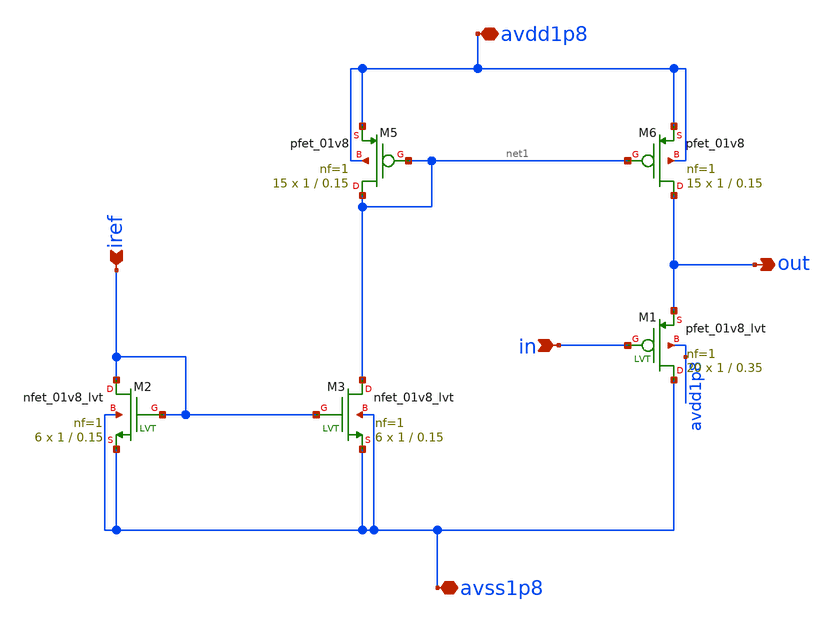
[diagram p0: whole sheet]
** sch_path: xschem/source_follower_buff_pmos.sch
**.subckt source_follower_buff_pmos avdd1p8 avss1p8 out in iref
*.iopin avdd1p8
*.iopin avss1p8
*.opin out
*.ipin in
*.ipin iref
XM5 net1 net1 avdd1p8 avdd1p8 sky130_fd_pr__pfet_01v8 L=0.15 W=1 nf=1 ad='int((nf+1)/2) * W/nf * 0.29'
+ as='int((nf+2)/2) * W/nf * 0.29' pd='2*int((nf+1)/2) * (W/nf + 0.29)' ps='2*int((nf+2)/2) * (W/nf + 0.29)'
+ nrd='0.29 / W' nrs='0.29 / W' sa=0 sb=0 sd=0 mult=15 m=15
XM6 out net1 avdd1p8 avdd1p8 sky130_fd_pr__pfet_01v8 L=0.15 W=1 nf=1 ad='int((nf+1)/2) * W/nf * 0.29'
+ as='int((nf+2)/2) * W/nf * 0.29' pd='2*int((nf+1)/2) * (W/nf + 0.29)' ps='2*int((nf+2)/2) * (W/nf + 0.29)'
+ nrd='0.29 / W' nrs='0.29 / W' sa=0 sb=0 sd=0 mult=15 m=15
XM1 avss1p8 in out avdd1p8 sky130_fd_pr__pfet_01v8_lvt L=0.35 W=1 nf=1 ad='int((nf+1)/2) * W/nf * 0.29'
+ as='int((nf+2)/2) * W/nf * 0.29' pd='2*int((nf+1)/2) * (W/nf + 0.29)' ps='2*int((nf+2)/2) * (W/nf + 0.29)'
+ nrd='0.29 / W' nrs='0.29 / W' sa=0 sb=0 sd=0 mult=20 m=20
XM2 iref iref avss1p8 avss1p8 sky130_fd_pr__nfet_01v8_lvt L=0.15 W=1 nf=1 ad='int((nf+1)/2) * W/nf * 0.29'
+ as='int((nf+2)/2) * W/nf * 0.29' pd='2*int((nf+1)/2) * (W/nf + 0.29)' ps='2*int((nf+2)/2) * (W/nf + 0.29)'
+ nrd='0.29 / W' nrs='0.29 / W' sa=0 sb=0 sd=0 mult=6 m=6
XM3 net1 iref avss1p8 avss1p8 sky130_fd_pr__nfet_01v8_lvt L=0.15 W=1 nf=1 ad='int((nf+1)/2) * W/nf * 0.29'
+ as='int((nf+2)/2) * W/nf * 0.29' pd='2*int((nf+1)/2) * (W/nf + 0.29)' ps='2*int((nf+2)/2) * (W/nf + 0.29)'
+ nrd='0.29 / W' nrs='0.29 / W' sa=0 sb=0 sd=0 mult=6 m=6
**.ends
.end
